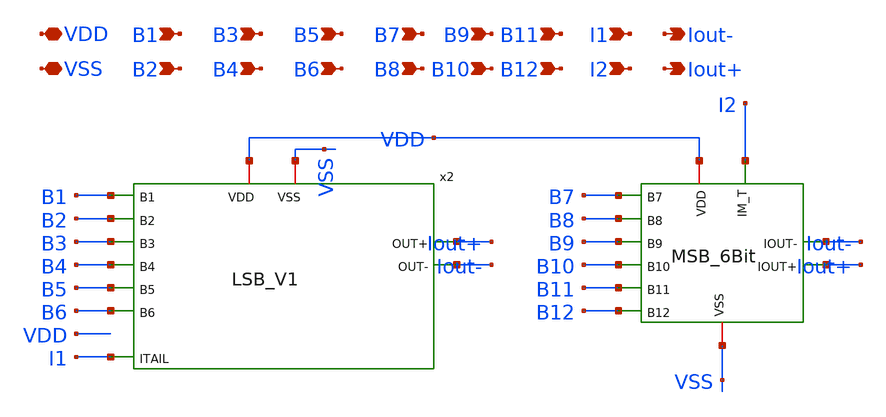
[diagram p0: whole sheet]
** sch_path: DAC_PAKISTAN_01/Pakistan1_Xschem/DAC_12Bit_V1.sch
**.subckt DAC_12Bit_V1 VDD VSS B1 B2 B3 B4 B5 B6 B7 B8 B9 B10 B11 B12 I1 I2 Iout- Iout+
*.iopin VDD
*.iopin VSS
*.ipin B1
*.ipin B2
*.ipin B3
*.ipin B4
*.ipin B5
*.ipin B6
*.ipin B7
*.ipin B8
*.ipin B9
*.ipin B10
*.ipin B11
*.ipin B12
*.ipin I1
*.ipin I2
*.opin Iout-
*.opin Iout+
x1 VSS VDD B11 B7 B8 B12 B9 I2 B10 Iout- Iout+ MSB_6Bit
x2 VDD VSS B1 B2 B3 B4 B5 B6 I1 Iout+ Iout- LSB_V1
**.ends
.end
